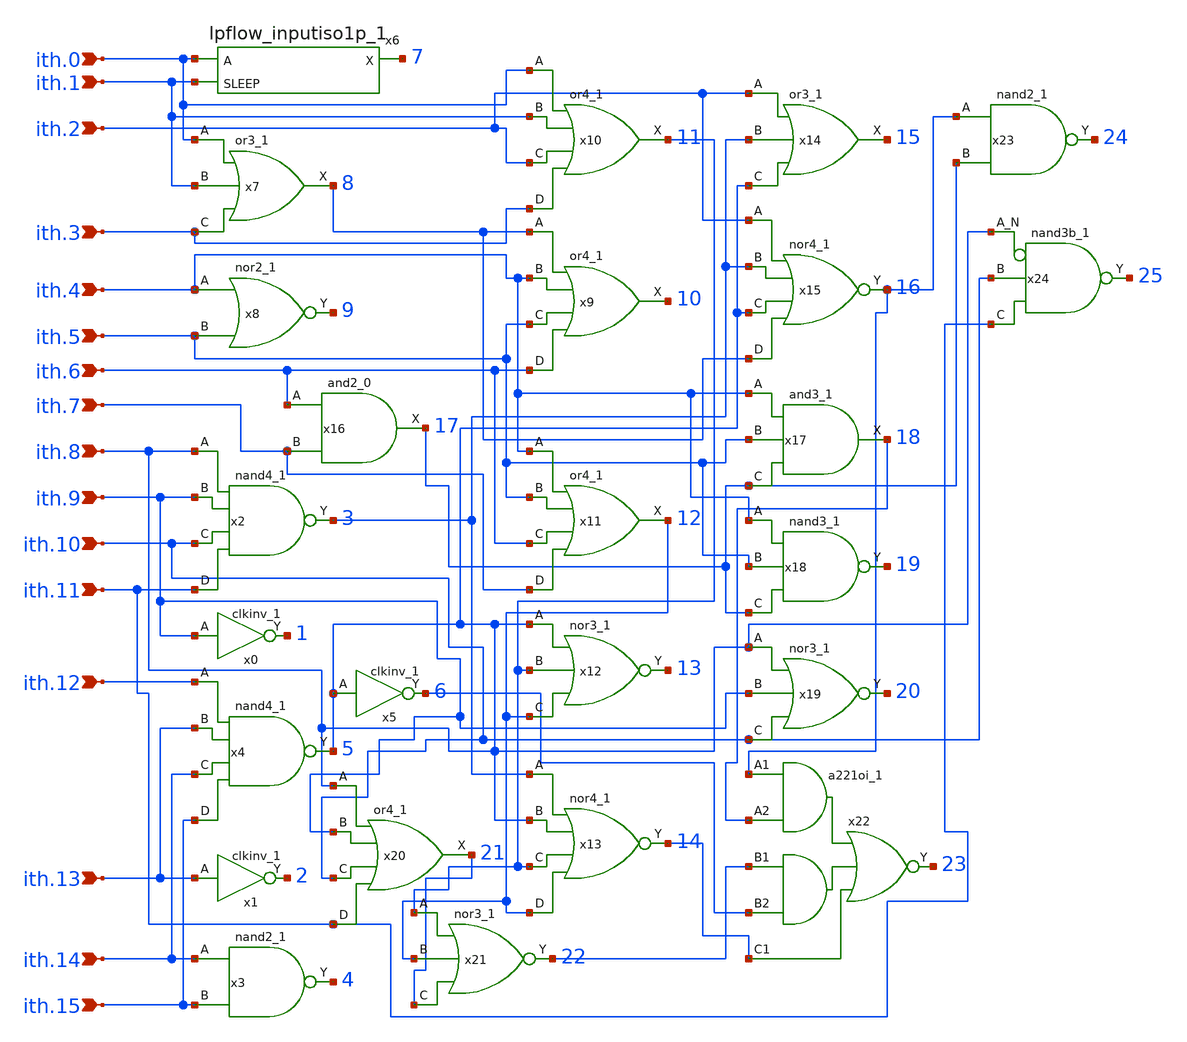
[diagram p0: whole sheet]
** sch_path: verilog/therm.sch
**.subckt therm ith.9 ith.13 ith.8 ith.10 ith.11 ith.14 ith.15 ith.12 ith.0 ith.1 ith.3 ith.4 ith.5
*+ ith.6 ith.2 ith.7
*.ipin ith.9
*.ipin ith.13
*.ipin ith.8
*.ipin ith.10
*.ipin ith.11
*.ipin ith.14
*.ipin ith.15
*.ipin ith.12
*.ipin ith.0
*.ipin ith.1
*.ipin ith.3
*.ipin ith.4
*.ipin ith.5
*.ipin ith.6
*.ipin ith.2
*.ipin ith.7
x0 ith.9 VGND VNB VPB VPWR 1 sky130_fd_sc_hd__clkinv_1
x1 ith.13 VGND VNB VPB VPWR 2 sky130_fd_sc_hd__clkinv_1
x2 ith.8 ith.9 ith.10 ith.11 VGND VNB VPB VPWR 3 sky130_fd_sc_hd__nand4_1
x3 ith.14 ith.15 VGND VNB VPB VPWR 4 sky130_fd_sc_hd__nand2_1
x4 ith.12 ith.13 ith.14 ith.15 VGND VNB VPB VPWR ith.8 sky130_fd_sc_hd__nand4_1
x5 ith.8 VGND VNB VPB VPWR 6 sky130_fd_sc_hd__clkinv_1
x6 ith.0 ith.1 VGND VNB VPB VPWR 7 sky130_fd_sc_hd__lpflow_inputiso1p_1
x7 ith.0 ith.1 ith.3 VGND VNB VPB VPWR 8 sky130_fd_sc_hd__or3_1
x8 ith.4 ith.5 VGND VNB VPB VPWR 9 sky130_fd_sc_hd__nor2_1
x9 8 ith.4 ith.5 ith.6 VGND VNB VPB VPWR 10 sky130_fd_sc_hd__or4_1
x10 ith.0 ith.1 ith.2 ith.3 VGND VNB VPB VPWR 11 sky130_fd_sc_hd__or4_1
x11 ith.4 ith.5 ith.6 ith.7 VGND VNB VPB VPWR 12 sky130_fd_sc_hd__or4_1
x12 ith.8 11 12 VGND VNB VPB VPWR 13 sky130_fd_sc_hd__nor3_1
x13 3 ith.8 11 12 VGND VNB VPB VPWR 14 sky130_fd_sc_hd__nor4_1
x14 ith.2 3 ith.8 VGND VNB VPB VPWR 15 sky130_fd_sc_hd__or3_1
x15 ith.2 3 ith.8 8 VGND VNB VPB VPWR 16 sky130_fd_sc_hd__nor4_1
x16 ith.6 ith.7 VGND VNB VPB VPWR 17 sky130_fd_sc_hd__and2_0
x17 ith.4 ith.5 17 VGND VNB VPB VPWR 18 sky130_fd_sc_hd__and3_1
x18 ith.4 ith.5 17 VGND VNB VPB VPWR 19 sky130_fd_sc_hd__nand3_1
x19 ith.8 ith.9 ith.10 VGND VNB VPB VPWR 20 sky130_fd_sc_hd__nor3_1
x20 ith.8 ith.9 ith.10 ith.11 VGND VNB VPB VPWR 21 sky130_fd_sc_hd__or4_1
x21 11 12 21 VGND VNB VPB VPWR 22 sky130_fd_sc_hd__nor3_1
x22 16 18 22 6 14 VGND VNB VPB VPWR 23 sky130_fd_sc_hd__a221oi_1
x23 16 17 VGND VNB VPB VPWR 24 sky130_fd_sc_hd__nand2_1
x24 ith.8 ith.10 ith.11 VGND VNB VPB VPWR 25 sky130_fd_sc_hd__nand3b_1
**.ends
.end
